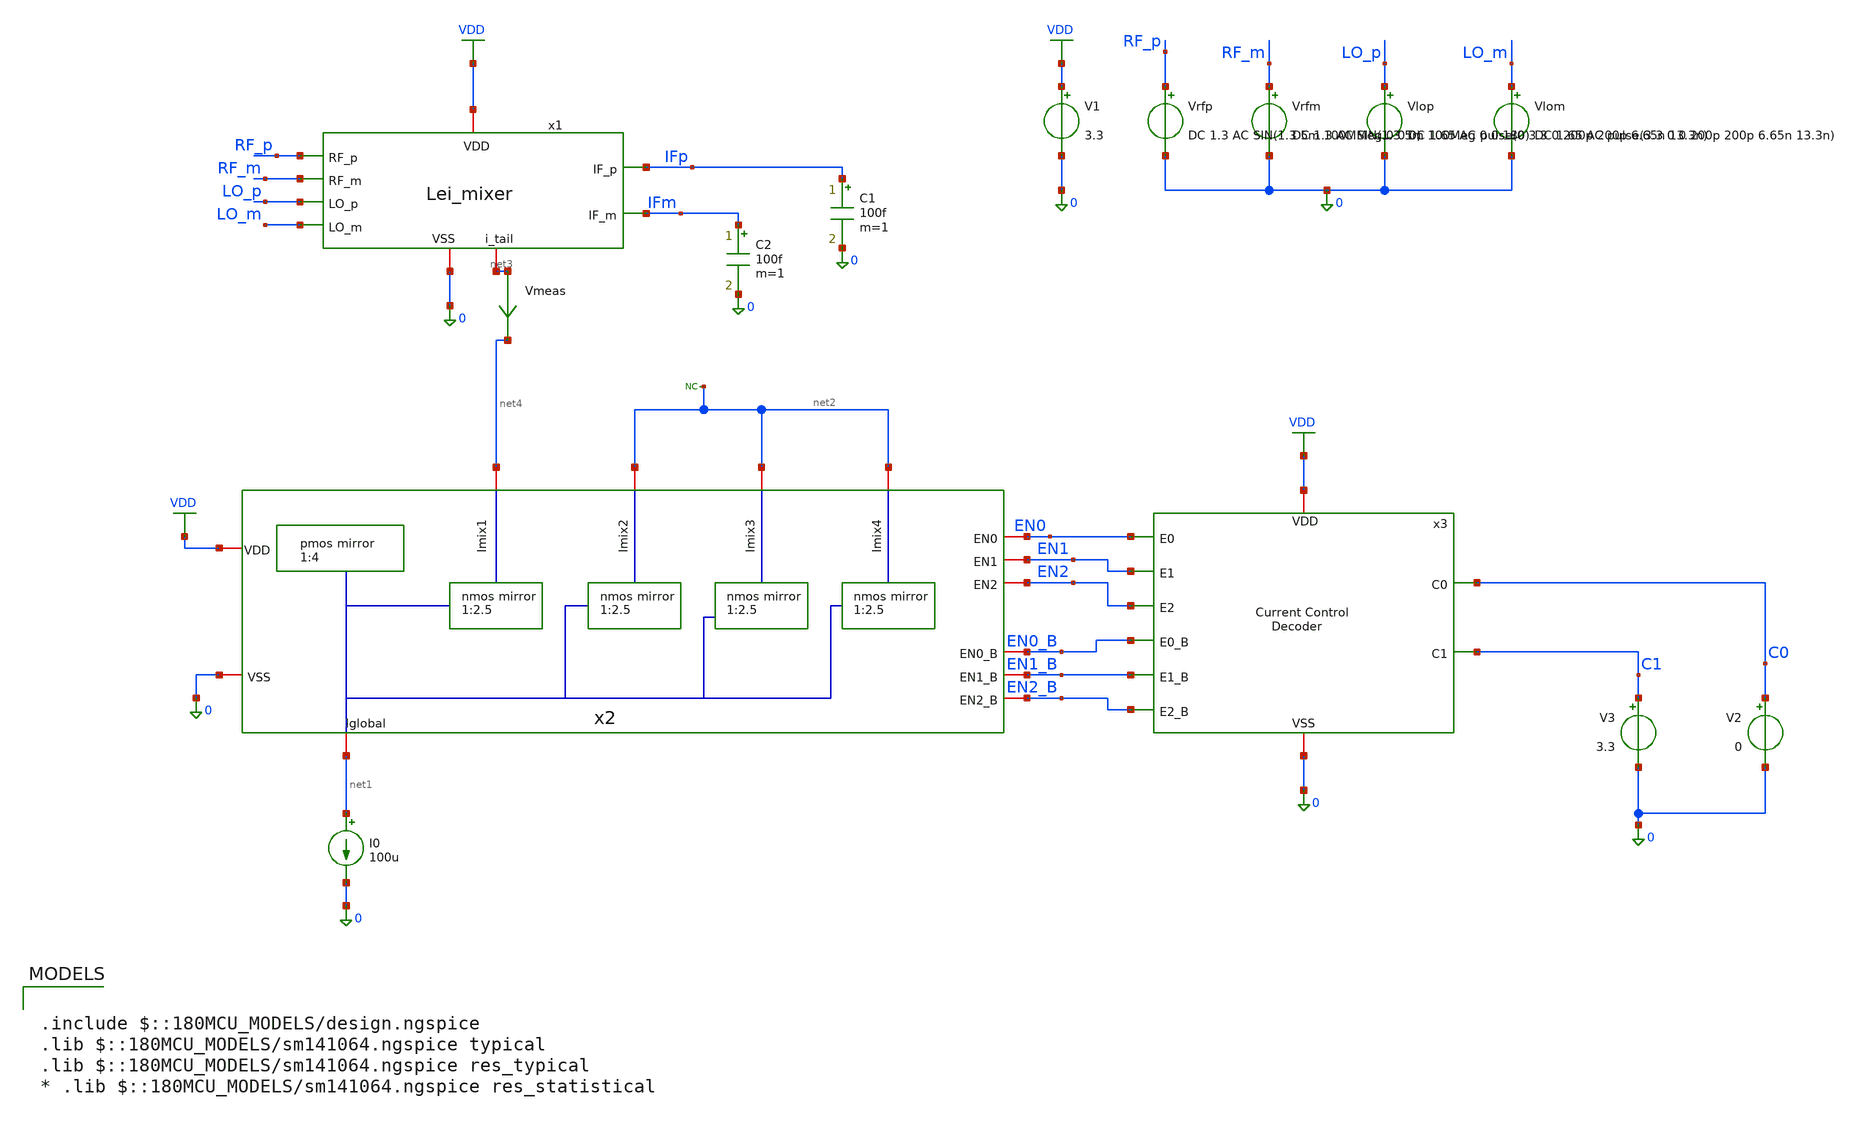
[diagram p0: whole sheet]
** sch_path: designs/mixer/testbench/Lei_mixer_with_mirror_en_tb.sch
**.subckt Lei_mixer_with_mirror_en_tb
V1 VDD 0 3.3
Vrfp RF_p 0 DC 1.3 AC SIN(1.3 5m 100MMeg 0 0 0)
Vrfm RF_m 0 DC 1.3 AC SIN(1.3 5m 100Meg 0 0 180)
Vlop LO_p 0 DC 1.65 AC pulse(0 3.3 0 200p 200p 6.65n 13.3n)
Vlom LO_m 0 DC 1.65 AC pulse(3.3 0 0 200p 200p 6.65n 13.3n)
C1 IFp 0 100f m=1
C2 IFm 0 100f m=1
I0 net1 0 100u
* noconn #net2
Vmeas net3 net4 0
.save i(vmeas)
x2 EN2 EN1 EN0 EN0_B EN1_B EN2_B VDD net1 net2 net4 0 net2 net2 mirror_network_with_enable
V2 C0 0 0
V3 C1 0 3.3
x3 VDD C0 EN2 C1 0 EN1 EN0 EN2_B EN1_B EN0_B decoder
x1 IFp RF_p VDD 0 IFm RF_m LO_p net3 LO_m Lei_mixer
**** begin user architecture code

.include $::180MCU_MODELS/design.ngspice
.lib $::180MCU_MODELS/sm141064.ngspice typical
.lib $::180MCU_MODELS/sm141064.ngspice res_typical
* .lib $::180MCU_MODELS/sm141064.ngspice res_statistical




.control

destroy all
save all
write mixer_tb.raw

op
echo RF pair
print @m.x1.xm1.m0[gm]
print @m.x1.xm1.m0[id]
print @m.x1.xm1.m0[vgs]
print @m.x1.xm1.m0[vds]
print @m.x1.xm1.m0[vdsat]

echo LO pair
print @m.x1.xm3.m0[gm]
print @m.x1.xm3.m0[id]
print @m.x1.xm3.m0[vgs]
print @m.x1.xm3.m0[vds]
print @m.x1.xm3.m0[vdsat]

echo nmos tail
print @m.x2.x2.xm2.m0[gm]
print @m.x2.x2.xm2.m0[id]
print @m.x2.x2.xm2.m0[vgs]
print @m.x2.x2.xm2.m0[vds]
print @m.x2.x2.xm2.m0[vdsat]

print i(vmeas)

tran 1n 2u ;transient sim
let vrf = V(RF_p)-V(RF_m)
let vif = V(IFp)-V(IFm)

plot V(LO_p)
plot vrf
plot vif

plot i(v.x1.v_i_ifp) i(v.x1.v_i_ifm) LO_P ifp xlimit 100n 140n

fft vif vrf

let vif_mag = mag(vif)

plot vdb(vif_mag) vs frequency xlimit 0 1G
.endc


**** end user architecture code
**.ends
.GLOBAL VDD
.end
